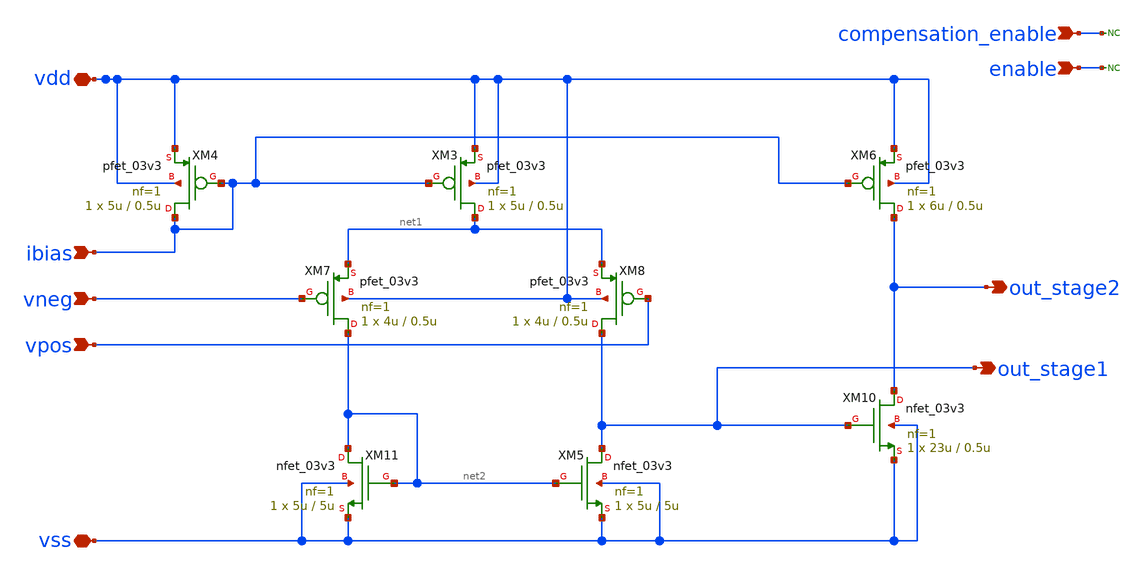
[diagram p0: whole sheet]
** sch_path: DESIGN/DACFUTURE_EDU/Two_stage_OTA/two_stage_ota.sch
**.subckt two_stage_ota enable vpos vneg vdd vss compensation_enable out_stage2 ibias
*.ipin enable
*.ipin vpos
*.ipin vneg
*.iopin vdd
*.iopin vss
*.ipin compensation_enable
*.opin out_stage2
*.ipin ibias
* noconn compensation_enable
* noconn enable
XM3 net1 ibias vdd vdd pfet_03v3 L=0.5u W=5u nf=1 ad='int((nf+1)/2) * W/nf * 0.18u' as='int((nf+2)/2) * W/nf * 0.18u'
+ pd='2*int((nf+1)/2) * (W/nf + 0.18u)' ps='2*int((nf+2)/2) * (W/nf + 0.18u)' nrd='0.18u / W' nrs='0.18u / W'
+ sa=0 sb=0 sd=0 m=1
XM4 ibias ibias vdd vdd pfet_03v3 L=0.5u W=5u nf=1 ad='int((nf+1)/2) * W/nf * 0.18u' as='int((nf+2)/2) * W/nf * 0.18u'
+ pd='2*int((nf+1)/2) * (W/nf + 0.18u)' ps='2*int((nf+2)/2) * (W/nf + 0.18u)' nrd='0.18u / W' nrs='0.18u / W'
+ sa=0 sb=0 sd=0 m=1
XM6 out_stage2 ibias vdd vdd pfet_03v3 L=0.5u W=6u nf=1 ad='int((nf+1)/2) * W/nf * 0.18u' as='int((nf+2)/2) * W/nf * 0.18u'
+ pd='2*int((nf+1)/2) * (W/nf + 0.18u)' ps='2*int((nf+2)/2) * (W/nf + 0.18u)' nrd='0.18u / W' nrs='0.18u / W'
+ sa=0 sb=0 sd=0 m=1
XM7 net2 vneg net1 vdd pfet_03v3 L=0.5u W=4u nf=1 ad='int((nf+1)/2) * W/nf * 0.18u' as='int((nf+2)/2) * W/nf * 0.18u'
+ pd='2*int((nf+1)/2) * (W/nf + 0.18u)' ps='2*int((nf+2)/2) * (W/nf + 0.18u)' nrd='0.18u / W' nrs='0.18u / W'
+ sa=0 sb=0 sd=0 m=1
XM8 out_stage1 vpos net1 vdd pfet_03v3 L=0.5u W=4u nf=1 ad='int((nf+1)/2) * W/nf * 0.18u' as='int((nf+2)/2) * W/nf * 0.18u'
+ pd='2*int((nf+1)/2) * (W/nf + 0.18u)' ps='2*int((nf+2)/2) * (W/nf + 0.18u)' nrd='0.18u / W' nrs='0.18u / W'
+ sa=0 sb=0 sd=0 m=1
XM5 out_stage1 net2 vss vss nfet_03v3 L=5u W=5u nf=1 ad='int((nf+1)/2) * W/nf * 0.18u' as='int((nf+2)/2) * W/nf * 0.18u'
+ pd='2*int((nf+1)/2) * (W/nf + 0.18u)' ps='2*int((nf+2)/2) * (W/nf + 0.18u)' nrd='0.18u / W' nrs='0.18u / W'
+ sa=0 sb=0 sd=0 m=1
XM10 out_stage2 out_stage1 vss vss nfet_03v3 L=0.5u W=23u nf=1 ad='int((nf+1)/2) * W/nf * 0.18u' as='int((nf+2)/2) * W/nf * 0.18u'
+ pd='2*int((nf+1)/2) * (W/nf + 0.18u)' ps='2*int((nf+2)/2) * (W/nf + 0.18u)' nrd='0.18u / W' nrs='0.18u / W'
+ sa=0 sb=0 sd=0 m=1
XM11 net2 net2 vss vss nfet_03v3 L=5u W=5u nf=1 ad='int((nf+1)/2) * W/nf * 0.18u' as='int((nf+2)/2) * W/nf * 0.18u'
+ pd='2*int((nf+1)/2) * (W/nf + 0.18u)' ps='2*int((nf+2)/2) * (W/nf + 0.18u)' nrd='0.18u / W' nrs='0.18u / W'
+ sa=0 sb=0 sd=0 m=1
**.ends
.end
